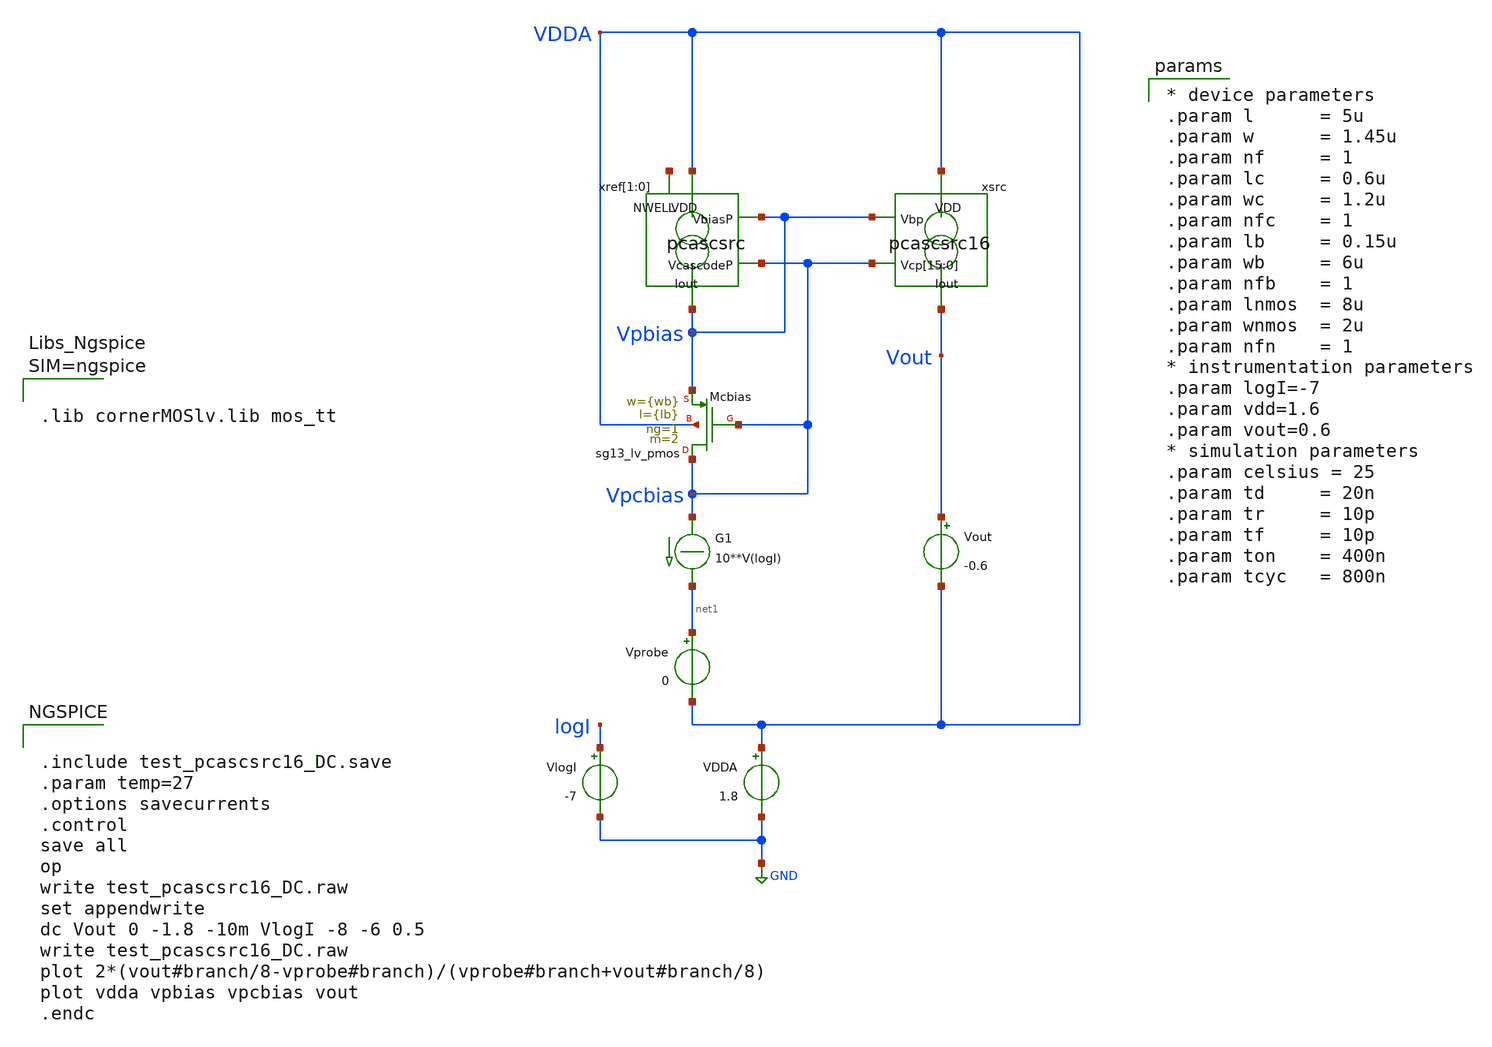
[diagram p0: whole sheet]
** sch_path: xschem/test_pcascsrc16_DC.sch
**.subckt test_pcascsrc16_DC
Vout Vout VDDA -0.6
.save i(vout)
Vprobe net1 VDDA 0
.save i(vprobe)
G1 Vpcbias net1 CUR=' 10**V(logI) '
VlogI logI GND -7
.save i(vlogi)
xref[1] VDDA Vpbias Vpcbias Vpbias net2[1] pcascsrc
xref[0] VDDA Vpbias Vpcbias Vpbias net2[0] pcascsrc
xsrc VDDA Vpbias Vpcbias Vpcbias Vpcbias Vpcbias Vpcbias Vpcbias Vpcbias Vpcbias Vpcbias Vpcbias Vpcbias
+ Vpcbias Vpcbias Vpcbias Vpcbias Vpcbias Vout pcascsrc16 l={l} w={w} lc={lc} wc={wc}
VDDA VDDA GND 1.8
.save i(vdda)
XMcbias Vpcbias Vpcbias Vpbias VDDA sg13_lv_pmos w={wb} l={lb} ng=1 m=2 mm_ok=1
**** begin user architecture code


.include test_pcascsrc16_DC.save
.param temp=27
.options savecurrents
.control
save all
op
write test_pcascsrc16_DC.raw
set appendwrite
dc Vout 0 -1.8 -10m VlogI -8 -6 0.5
write test_pcascsrc16_DC.raw
plot 2*(vout#branch/8-vprobe#branch)/(vprobe#branch+vout#branch/8)
plot vdda vpbias vpcbias vout
.endc





.lib cornerMOSlv.lib mos_tt




* device parameters
.param l      = 5u
.param w      = 1.45u
.param nf     = 1
.param lc     = 0.6u
.param wc     = 1.2u
.param nfc    = 1
.param lb     = 0.15u
.param wb     = 6u
.param nfb    = 1
.param lnmos  = 8u
.param wnmos  = 2u
.param nfn    = 1
* instrumentation parameters
.param logI=-7
.param vdd=1.6
.param vout=0.6
* simulation parameters
.param celsius = 25
.param td     = 20n
.param tr     = 10p
.param tf     = 10p
.param ton    = 400n
.param tcyc   = 800n


**** end user architecture code
**.ends

* expanding   symbol:  pcascsrc.sym # of pins=5
** sym_path: xschem/pcascsrc.sym
** sch_path: xschem/pcascsrc.sch
.subckt pcascsrc VDD VbiasP VcascodeP Iout NWELL
*.ipin VcascodeP
*.ipin VbiasP
*.opin Iout
*.ipin VDD
*.iopin NWELL
XMsrc drain VbiasP VDD NWELL sg13_lv_pmos w=0.74u l=2u ng=1 m=1 mm_ok=1
XMcasc Iout VcascodeP drain NWELL sg13_lv_pmos w=0.3u l=0.3u ng=1 m=1 mm_ok=1
.ends


* expanding   symbol:  pcascsrc16.sym # of pins=4
** sym_path: pcascsrc16.sym
** sch_path: pcascsrc16.sch
.subckt pcascsrc16 VDD Vbp Vcp[15] Vcp[14] Vcp[13] Vcp[12] Vcp[11] Vcp[10] Vcp[9] Vcp[8] Vcp[7]
+ Vcp[6] Vcp[5] Vcp[4] Vcp[3] Vcp[2] Vcp[1] Vcp[0] Iout  l=2u w=.74u lc=.3u wc=.3u
*.ipin
*+ Vcp[15],Vcp[14],Vcp[13],Vcp[12],Vcp[11],Vcp[10],Vcp[9],Vcp[8],Vcp[7],Vcp[6],Vcp[5],Vcp[4],Vcp[3],Vcp[2],Vcp[1],Vcp[0]
*.ipin Vbp
*.opin Iout
*.ipin VDD
xsrc[15] VDD Vbp Vcp[15] Iout net1[15] pcascsrc
xsrc[14] VDD Vbp Vcp[14] Iout net1[14] pcascsrc
xsrc[13] VDD Vbp Vcp[13] Iout net1[13] pcascsrc
xsrc[12] VDD Vbp Vcp[12] Iout net1[12] pcascsrc
xsrc[11] VDD Vbp Vcp[11] Iout net1[11] pcascsrc
xsrc[10] VDD Vbp Vcp[10] Iout net1[10] pcascsrc
xsrc[9] VDD Vbp Vcp[9] Iout net1[9] pcascsrc
xsrc[8] VDD Vbp Vcp[8] Iout net1[8] pcascsrc
xsrc[7] VDD Vbp Vcp[7] Iout net1[7] pcascsrc
xsrc[6] VDD Vbp Vcp[6] Iout net1[6] pcascsrc
xsrc[5] VDD Vbp Vcp[5] Iout net1[5] pcascsrc
xsrc[4] VDD Vbp Vcp[4] Iout net1[4] pcascsrc
xsrc[3] VDD Vbp Vcp[3] Iout net1[3] pcascsrc
xsrc[2] VDD Vbp Vcp[2] Iout net1[2] pcascsrc
xsrc[1] VDD Vbp Vcp[1] Iout net1[1] pcascsrc
xsrc[0] VDD Vbp Vcp[0] Iout net1[0] pcascsrc
.ends

.GLOBAL GND
.end
